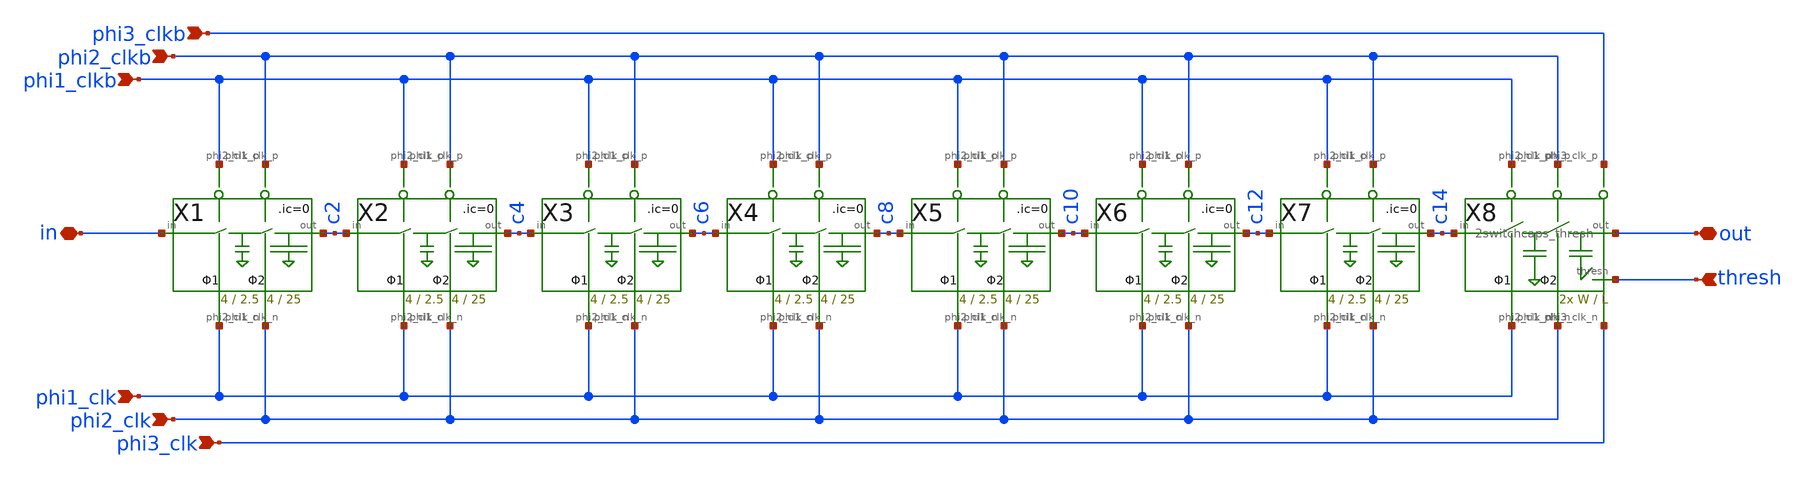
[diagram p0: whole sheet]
** sch_path: xschem/Switched_Caps/16switchcaps_2phi_thresh.sch
**.subckt 16switchcaps_2phi_thresh in out phi2_clkb phi1_clkb phi2_clk phi1_clk thresh phi3_clkb
*+ phi3_clk
*.iopin in
*.iopin out
*.ipin phi2_clkb
*.ipin phi1_clkb
*.ipin phi2_clk
*.ipin phi1_clk
*.ipin thresh
*.ipin phi3_clkb
*.ipin phi3_clk
X1 in c2 phi2_clk phi1_clk phi1_clkb phi2_clkb 2switchcaps Wcap1=4 Lcap1=2.5 Wcap2=4 Lcap2=25
X2 c2 c4 phi2_clk phi1_clk phi1_clkb phi2_clkb 2switchcaps Wcap1=4 Lcap1=2.5 Wcap2=4 Lcap2=25
X3 c4 c6 phi2_clk phi1_clk phi1_clkb phi2_clkb 2switchcaps Wcap1=4 Lcap1=2.5 Wcap2=4 Lcap2=25
X4 c6 c8 phi2_clk phi1_clk phi1_clkb phi2_clkb 2switchcaps Wcap1=4 Lcap1=2.5 Wcap2=4 Lcap2=25
X5 c8 c10 phi2_clk phi1_clk phi1_clkb phi2_clkb 2switchcaps Wcap1=4 Lcap1=2.5 Wcap2=4 Lcap2=25
X6 c10 c12 phi2_clk phi1_clk phi1_clkb phi2_clkb 2switchcaps Wcap1=4 Lcap1=2.5 Wcap2=4 Lcap2=25
X7 c12 c14 phi2_clk phi1_clk phi1_clkb phi2_clkb 2switchcaps Wcap1=4 Lcap1=2.5 Wcap2=4 Lcap2=25
X8 c14 out phi2_clk phi1_clk phi1_clkb phi2_clkb thresh phi3_clkb phi3_clk 2switchcaps_thresh Wcap=W
+ Lcap=L
**.ends

* expanding   symbol:  Switched_Caps/2switchcaps.sym # of pins=6
** sym_path: xschem/Switched_Caps/2switchcaps.sym
** sch_path: xschem/Switched_Caps/2switchcaps.sch
.subckt 2switchcaps in out phi2_clk_n phi1_clk_n phi1_clk_p phi2_clk_p  Wcap1=4 Lcap1=2.5 Wcap2=4
+ Lcap2=25
*.iopin out
*.iopin in
*.ipin phi1_clk_n
*.ipin phi1_clk_p
*.ipin phi2_clk_p
*.ipin phi2_clk_n
XC1 c1 GND sky130_fd_pr__cap_mim_m3_1 W=Wcap L=Lcap MF=1 m=1
XC2 out GND sky130_fd_pr__cap_mim_m3_1 W=Wcap L=Lcap MF=1 m=1
**** begin user architecture code

.ic v(c1)=0 v(out)=0

**** end user architecture code
X1 in c1 phi1_clk_p phi1_clk_n transmission_gate Wpmos=3 Lpmos=0.18 Wnmos=1 Lnmos=0.18
X2 c1 out phi2_clk_p phi2_clk_n transmission_gate Wpmos=3 Lpmos=0.18 Wnmos=1 Lnmos=0.18
.ends


* expanding   symbol:  Switched_Caps/2switchcaps_thresh.sym # of pins=9
** sym_path: xschem/Switched_Caps/2switchcaps_thresh.sym
** sch_path: xschem/Switched_Caps/2switchcaps_thresh.sch
.subckt 2switchcaps_thresh in out phi2_clk_n phi1_clk_n phi1_clk_p phi2_clk_p thresh phi3_clk_p
+ phi3_clk_n  Wcap=20 Lcap=20
*.iopin out
*.iopin in
*.ipin phi1_clk_n
*.ipin phi1_clk_p
*.ipin phi2_clk_p
*.ipin phi2_clk_n
*.ipin thresh
*.ipin phi3_clk_n
*.ipin phi3_clk_p
XC1 c1 GND sky130_fd_pr__cap_mim_m3_1 W=Wcap L=Lcap MF=1 m=1
X1 in c1 phi1_clk_p phi1_clk_n transmission_gate Wpmos=1 Lpmos=0.18 Wnmos=1 Lnmos=0.18
X2 c1 out phi2_clk_p phi2_clk_n transmission_gate Wpmos=1 Lpmos=0.18 Wnmos=1 Lnmos=0.18
XC2 out c2b sky130_fd_pr__cap_mim_m3_1 W=Wcap L=Lcap MF=1 m=1
**** begin user architecture code

.ic v(c1)=0 v(out)=0 v(c2b)=0

**** end user architecture code
X3 c2b thresh phi3_clk_p phi3_clk_n transmission_gate Wpmos=1 Lpmos=0.18 Wnmos=1 Lnmos=0.18
.ends


* expanding   symbol:  transmission_gate/transmission_gate.sym # of pins=4
** sym_path: xschem/transmission_gate/transmission_gate.sym
** sch_path: xschem/transmission_gate/transmission_gate.sch
.subckt transmission_gate in out ctrl_ ctrl  Wpmos=1 Lpmos=0.18 Wnmos=1 Lnmos=0.18
*.iopin in
*.iopin out
*.ipin ctrl_
*.ipin ctrl
XM1 in ctrl out GND sky130_fd_pr__nfet_01v8 L=Lnmos W=Wnmos nf=1 ad='int((nf+1)/2) * W/nf * 0.29' as='int((nf+2)/2) * W/nf * 0.29'
+ pd='2*int((nf+1)/2) * (W/nf + 0.29)' ps='2*int((nf+2)/2) * (W/nf + 0.29)' nrd='0.29 / W' nrs='0.29 / W'
+ sa=0 sb=0 sd=0 mult=1 m=1
XM2 out ctrl_ in VDD sky130_fd_pr__pfet_01v8 L=Lpmos W=Wpmos nf=1 ad='int((nf+1)/2) * W/nf * 0.29' as='int((nf+2)/2) * W/nf * 0.29'
+ pd='2*int((nf+1)/2) * (W/nf + 0.29)' ps='2*int((nf+2)/2) * (W/nf + 0.29)' nrd='0.29 / W' nrs='0.29 / W'
+ sa=0 sb=0 sd=0 mult=1 m=1
.ends

.GLOBAL GND
.GLOBAL VDD
.end
